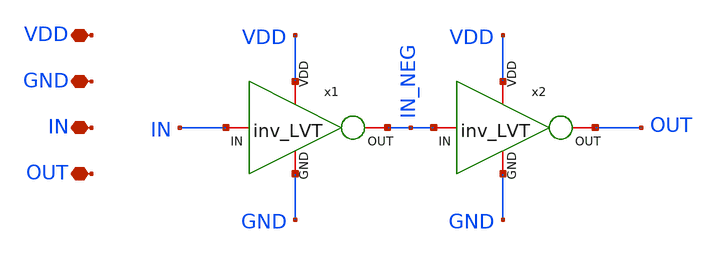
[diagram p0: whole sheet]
** sch_path: LVT/Buffer/Buffer.sch
**.subckt Buffer VDD GND IN OUT
*.iopin VDD
*.iopin GND
*.iopin IN
*.iopin OUT
x1 VDD IN IN_NEG GND inv_LVT
x2 VDD IN_NEG OUT GND inv_LVT
**.ends

* expanding   symbol:  /foss/designs/RO_Aging_UNICASS/LVT/inv_LVT/inv_LVT.sym # of pins=4
** sym_path: LVT/inv_LVT.sym
** sch_path: LVT/inv_LVT.sch
.subckt inv_LVT VDD IN OUT GND
*.iopin VDD
*.iopin IN
*.iopin OUT
*.iopin GND
XM1 OUT IN GND GND sky130_fd_pr__nfet_01v8_lvt L=0.15 W=0.45 nf=1 ad='int((nf+1)/2) * W/nf * 0.29' as='int((nf+2)/2) * W/nf * 0.29'
+ pd='2*int((nf+1)/2) * (W/nf + 0.29)' ps='2*int((nf+2)/2) * (W/nf + 0.29)' nrd='0.29 / W' nrs='0.29 / W'
+ sa=0 sb=0 sd=0 mult=1 m=1
XM2 OUT IN VDD VDD sky130_fd_pr__pfet_01v8_lvt L=0.35 W=0.9 nf=1 ad='int((nf+1)/2) * W/nf * 0.29' as='int((nf+2)/2) * W/nf * 0.29'
+ pd='2*int((nf+1)/2) * (W/nf + 0.29)' ps='2*int((nf+2)/2) * (W/nf + 0.29)' nrd='0.29 / W' nrs='0.29 / W'
+ sa=0 sb=0 sd=0 mult=1 m=1
.ends

.end
